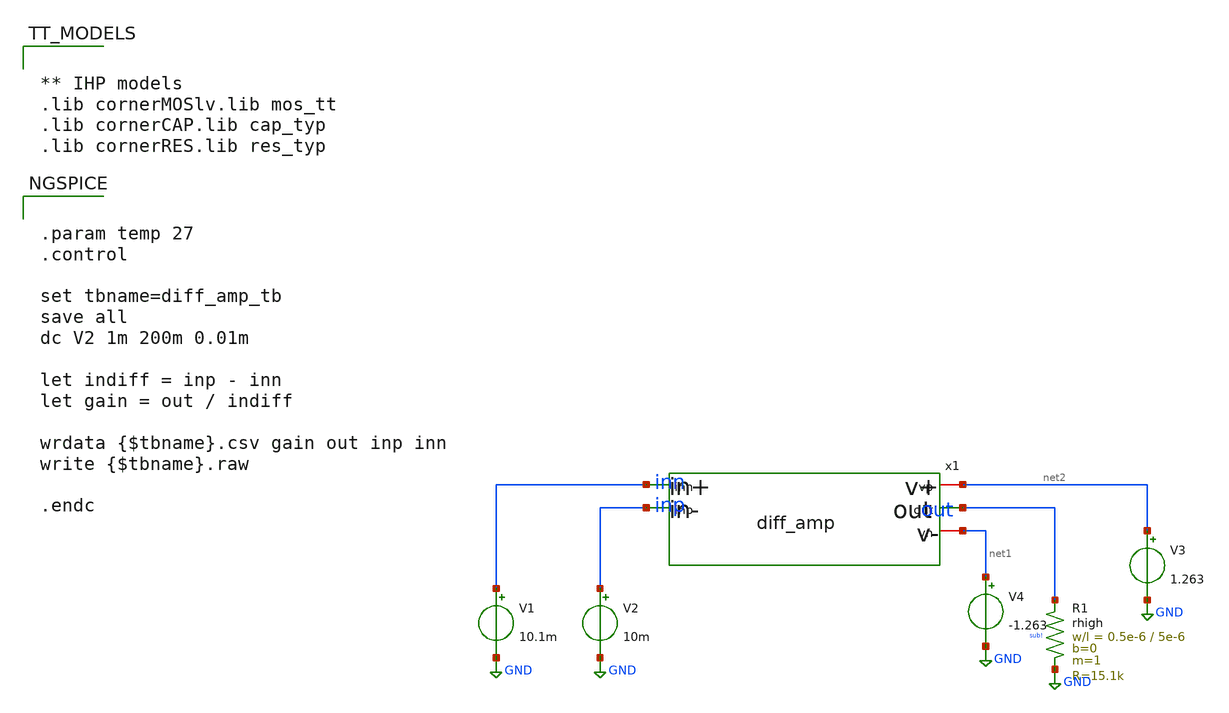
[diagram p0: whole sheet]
** sch_path: TempSensor/design_data/xschem/diff_amp_tb.sch
**.subckt diff_amp_tb
V1 inn GND 10.1m
V2 inp GND 10m
V3 net2 GND 1.263
x1 net2 inn inp out net1 diff_amp
XR1 out GND sub! rhigh w=0.5e-6 l=5e-6 m=1 b=0 mm_ok=1
V4 net1 GND -1.263
**** begin user architecture code


** IHP models
.lib cornerMOSlv.lib mos_tt
.lib cornerCAP.lib cap_typ
.lib cornerRES.lib res_typ




.param temp 27
.control

set tbname=diff_amp_tb
save all
dc V2 1m 200m 0.01m

let indiff = inp - inn
let gain = out / indiff

wrdata {$tbname}.csv gain out inp inn
write {$tbname}.raw

.endc


**** end user architecture code
**.ends

* expanding   symbol:  practicing/TempSensor/design_data/xschem/diff_amp.sym # of pins=5
** sym_path: TempSensor/design_data/xschem/diff_amp.sym
** sch_path: TempSensor/design_data/xschem/diff_amp.sch
.subckt diff_amp vp inn inp out vn
*.ipin inp
*.opin out
*.ipin inn
*.iopin vn
*.iopin vp
XM6 net10 inn net2 vn sg13_lv_nmos w=10u l=0.5u ng=1 m=1 mm_ok=1
XM5 net11 inp net2 vn sg13_lv_nmos w=10u l=0.5u ng=1 m=1 mm_ok=1
XM2 net1 net1 net4 vp sg13_lv_pmos w=10u l=2u ng=1 m=10 mm_ok=1
XM1 net4 net1 vp vp sg13_lv_pmos w=6u l=1u ng=1 m=1 mm_ok=1
XM3 net3 net1 vp vp sg13_lv_pmos w=6u l=1u ng=1 m=1 mm_ok=1
XM4 net5 net1 net3 vp sg13_lv_pmos w=10u l=2u ng=1 m=10 mm_ok=1
XM7 net5 net5 net6 vn sg13_lv_nmos w=10u l=2u ng=1 m=10 mm_ok=1
XM8 net6 net5 vn vn sg13_lv_nmos w=10u l=5u ng=1 m=1 mm_ok=1
XM9 net2 net5 net7 vn sg13_lv_nmos w=10u l=2u ng=1 m=10 mm_ok=1
XM10 net7 net5 vn vn sg13_lv_nmos w=10u l=5u ng=1 m=1 mm_ok=1
XM15 net8 net8 vn vn sg13_lv_nmos w=10u l=1.5u ng=1 m=1 mm_ok=1
XM16 net9 net8 vn vn sg13_lv_nmos w=10u l=1.5u ng=1 m=1 mm_ok=1
XM11 net10 net1 vp vp sg13_lv_pmos w=10u l=1.67u ng=1 m=1 mm_ok=1
XM12 net8 net1 net10 vp sg13_lv_pmos w=10u l=2u ng=1 m=10 mm_ok=1
XM13 net11 net1 vp vp sg13_lv_pmos w=10u l=1.67u ng=1 m=1 mm_ok=1
XM14 net9 net1 net11 vp sg13_lv_pmos w=10u l=2u ng=1 m=10 mm_ok=1
XM17 out net1 vp vp sg13_lv_pmos w=9u l=5u ng=1 m=10 mm_ok=1
XM18 out net9 vn vn sg13_lv_nmos w=10u l=0.5u ng=1 m=5 mm_ok=1
I0 net1 vn 20u
XC2 net9 out cap_cmim w=35e-6 l=35e-6 m=1 mm_ok=1
.ends

.GLOBAL GND
.end
